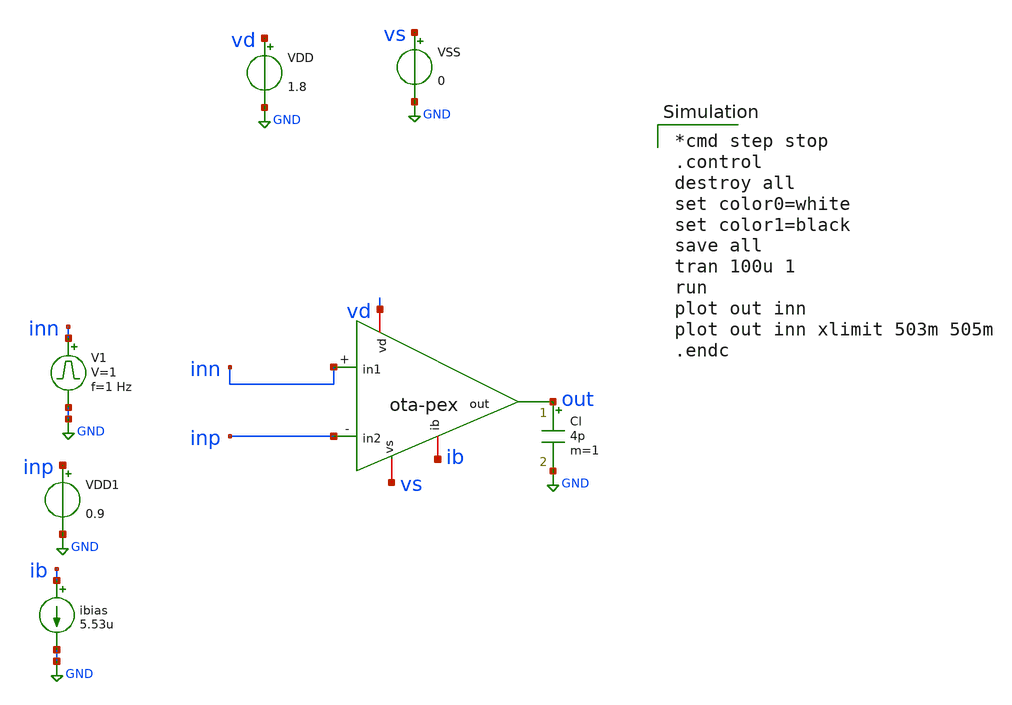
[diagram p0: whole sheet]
** sch_path: ota/xschem/ota_tb-largesignal.sch
* Copyright 2020 Stefan Frederik Schippers
* Licensed under the Apache License, Version 2.0 (the "License");
* you may not use this file except in compliance with the License.
* You may obtain a copy of the License at
* https://www.apache.org/licenses/LICENSE-2.0
* Unless required by applicable law or agreed to in writing, software
* distributed under the License is distributed on an "AS IS" BASIS,
* WITHOUT WARRANTIES OR CONDITIONS OF ANY KIND, either express or implied.
* See the License for the specific language governing permissions and
* limitations under the License.
**.subckt ota_tb-largesignal
ibias ib GND 5.53u
VDD vd GND 1.8
VSS vs GND 0
V1 inn GND pulse 0 1 '0.495/ 1 ' '0.01/1 ' '0.01/1 ' '0.49/1 ' '1/1 '
Cl out GND 4p m=1
VDD1 inp GND 0.9
X1 vd ib out inp inn vs ota-pex
**** begin user architecture code

*cmd step stop
.control
destroy all
set color0=white
set color1=black
save all
tran 100u 1
run
plot out inn
plot out inn xlimit 503m 505m
.endc

 .lib $::SKYWATER_MODELS/sky130.lib.spice tt
.include $::SKYWATER_STDCELLS/sky130_fd_sc_hd.spice

**** end user architecture code
**.ends
.GLOBAL GND
.end
